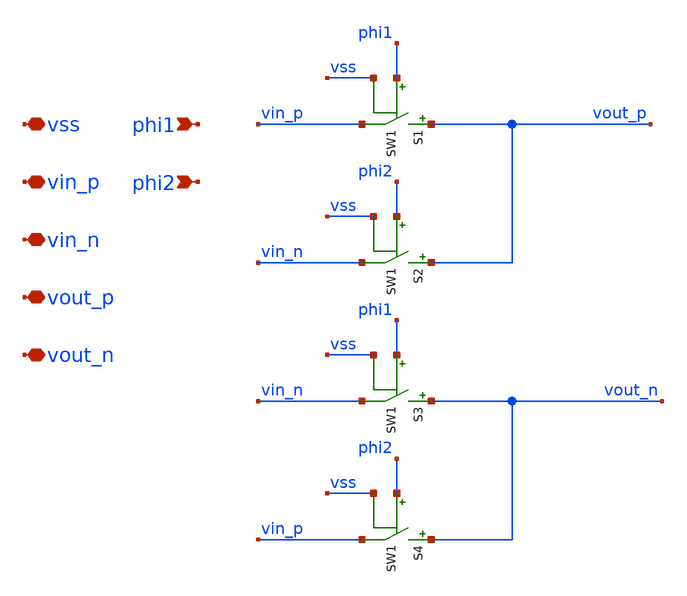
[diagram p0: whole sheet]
** sch_path: xschem/archive/chopper_bhv/chopper_bhv.sch
**.subckt chopper_bhv vss vin_p vin_n vout_p vout_n phi1 phi2
*.iopin vss
*.iopin vin_p
*.iopin vin_n
*.iopin vout_p
*.iopin vout_n
*.ipin phi1
*.ipin phi2
S1 vout_p vin_p phi1 vss SW1
S2 vout_p vin_n phi2 vss SW1
S3 vout_n vin_n phi1 vss SW1
S4 vout_n vin_p phi2 vss SW1
**.ends
**** begin user architecture code
.MODEL SW1 SW   VT=1.65 VH=0  RON=1 ROFF=1G
**** end user architecture code
.end
